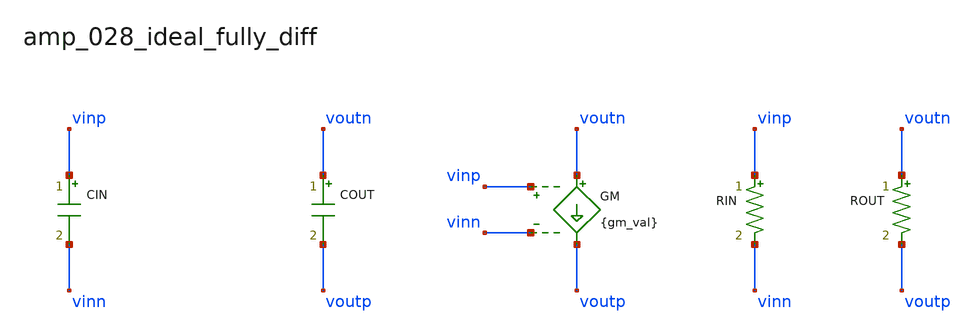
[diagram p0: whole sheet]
** sch_path: analog-db/raw/amp_028_ideal_fully_diff/hier/amp_028_ideal_fully_diff.sch
**.subckt amp_028_ideal_fully_diff
CIN vinp vinn 'cin_val' m=1
COUT voutn voutp 'cout_val' m=1
GM voutn voutp vinp vinn {gm_val}
RIN vinp vinn 'rin_val' m=1
ROUT voutn voutp 'rout_val' m=1
**.ends
.end
